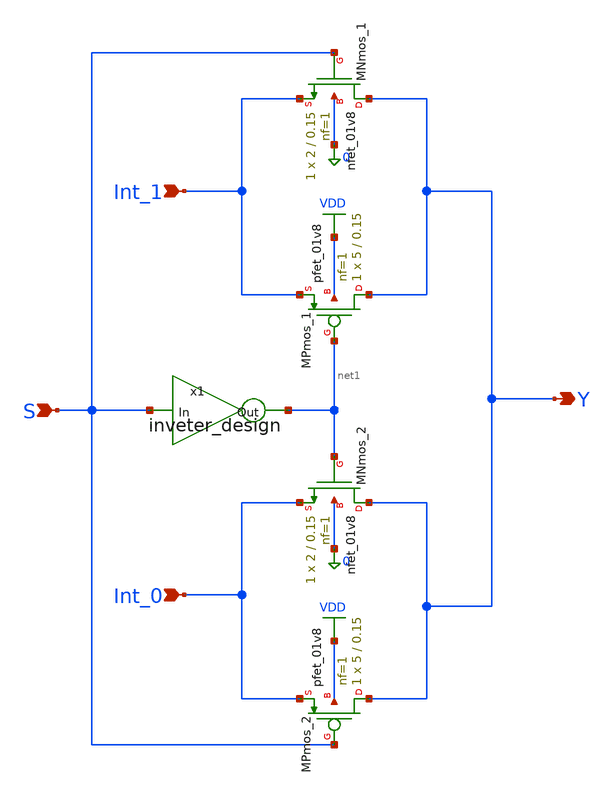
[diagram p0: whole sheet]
** sch_path: cells/full_adder_tg/xschem/mux_2to1_design.sch
**.subckt mux_2to1_design Int_1 Int_0 Y S
*.ipin Int_1
*.ipin Int_0
*.opin Y
*.ipin S
XMNmos_1 Y S Int_1 0 sky130_fd_pr__nfet_01v8 L=0.15 W=2 nf=1 ad='int((1 + 1)/2) * 2 / 1 * 0.29' as='int((1 + 2)/2) * 2 / 1 * 0.29'
+ pd='2*int((1 + 1)/2) * (2 / 1 + 0.29)' ps='2*int((1 + 2)/2) * (2 / 1 + 0.29)' nrd='0.29 / 2 ' nrs='0.29 / 2 '
+ sa=0 sb=0 sd=0 mult=1 m=1
XMPmos_1 Y net1 Int_1 VDD sky130_fd_pr__pfet_01v8 L=0.15 W=5 nf=1 ad='int((1 + 1)/2) * 5 / 1 * 0.29'
+ as='int((1 + 2)/2) * 5 / 1 * 0.29' pd='2*int((1 + 1)/2) * (5 / 1 + 0.29)' ps='2*int((1 + 2)/2) * (5 / 1 + 0.29)'
+ nrd='0.29 / 5 ' nrs='0.29 / 5 ' sa=0 sb=0 sd=0 mult=1 m=1
XMNmos_2 Y net1 Int_0 0 sky130_fd_pr__nfet_01v8 L=0.15 W=2 nf=1 ad='int((1 + 1)/2) * 2 / 1 * 0.29' as='int((1 + 2)/2) * 2 / 1 * 0.29'
+ pd='2*int((1 + 1)/2) * (2 / 1 + 0.29)' ps='2*int((1 + 2)/2) * (2 / 1 + 0.29)' nrd='0.29 / 2 ' nrs='0.29 / 2 '
+ sa=0 sb=0 sd=0 mult=1 m=1
XMPmos_2 Y S Int_0 VDD sky130_fd_pr__pfet_01v8 L=0.15 W=5 nf=1 ad='int((1 + 1)/2) * 5 / 1 * 0.29' as='int((1 + 2)/2) * 5 / 1 * 0.29'
+ pd='2*int((1 + 1)/2) * (5 / 1 + 0.29)' ps='2*int((1 + 2)/2) * (5 / 1 + 0.29)' nrd='0.29 / 5 ' nrs='0.29 / 5 '
+ sa=0 sb=0 sd=0 mult=1 m=1
x1 net1 S inveter_design
**.ends

* expanding   symbol:  ./inveter_design.sym # of pins=2
** sym_path: cells/full_adder_tg/xschem/inveter_design.sym
** sch_path: cells/full_adder_tg/xschem/inveter_design.sch
.subckt inveter_design Out In
*.ipin In
*.opin Out
XMNMOS Out In 0 0 sky130_fd_pr__nfet_01v8 L=0.15 W=2 nf=1 ad='int((1 + 1)/2) * 2 / 1 * 0.29' as='int((1 + 2)/2) * 2 / 1 * 0.29'
+ pd='2*int((1 + 1)/2) * (2 / 1 + 0.29)' ps='2*int((1 + 2)/2) * (2 / 1 + 0.29)' nrd='0.29 / 2 ' nrs='0.29 / 2 '
+ sa=0 sb=0 sd=0 mult=1 m=1
XMPMOS Out In VDD VDD sky130_fd_pr__pfet_01v8 L=0.15 W=5 nf=1 ad='int((1 + 1)/2) * 5 / 1 * 0.29' as='int((1 + 2)/2) * 5 / 1 * 0.29'
+ pd='2*int((1 + 1)/2) * (5 / 1 + 0.29)' ps='2*int((1 + 2)/2) * (5 / 1 + 0.29)' nrd='0.29 / 5 ' nrs='0.29 / 5 '
+ sa=0 sb=0 sd=0 mult=1 m=1
.ends

.GLOBAL VDD
.end
